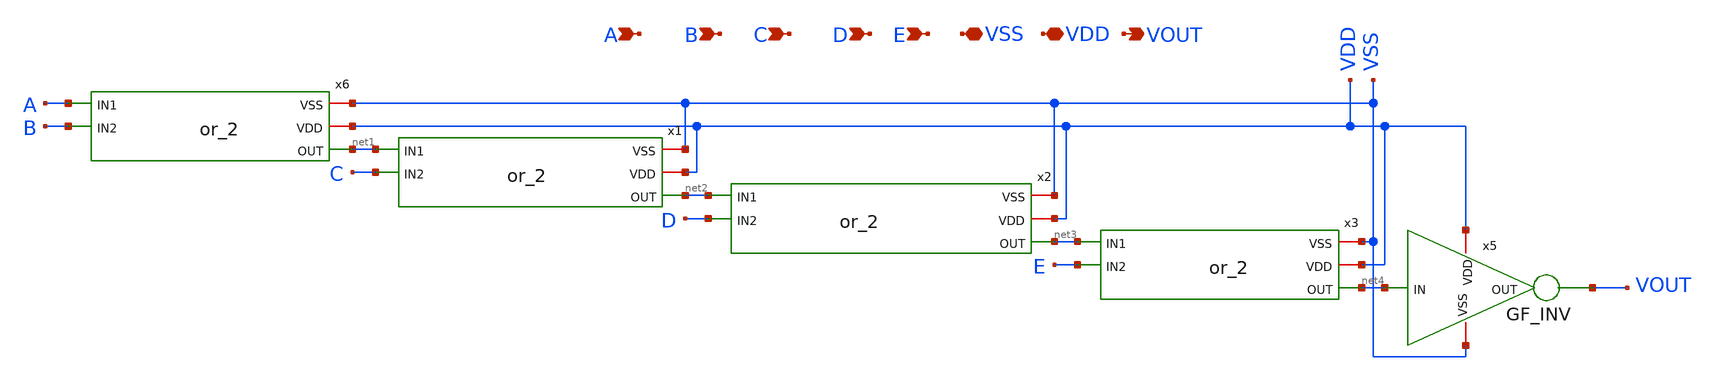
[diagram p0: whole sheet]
** sch_path: Clock_Generator_PAKISTAN_02/Schematics/nor_5.sch
**.subckt nor_5 B VSS VDD A VOUT D C E
*.ipin B
*.iopin VSS
*.iopin VDD
*.ipin A
*.opin VOUT
*.ipin D
*.ipin C
*.ipin E
x5 VSS VDD VOUT net4 GF_INV
x6 A VSS VDD net1 B or_2
x1 net1 VSS VDD net2 C or_2
x2 net2 VSS VDD net3 D or_2
x3 net3 VSS VDD net4 E or_2
**.ends
.end
